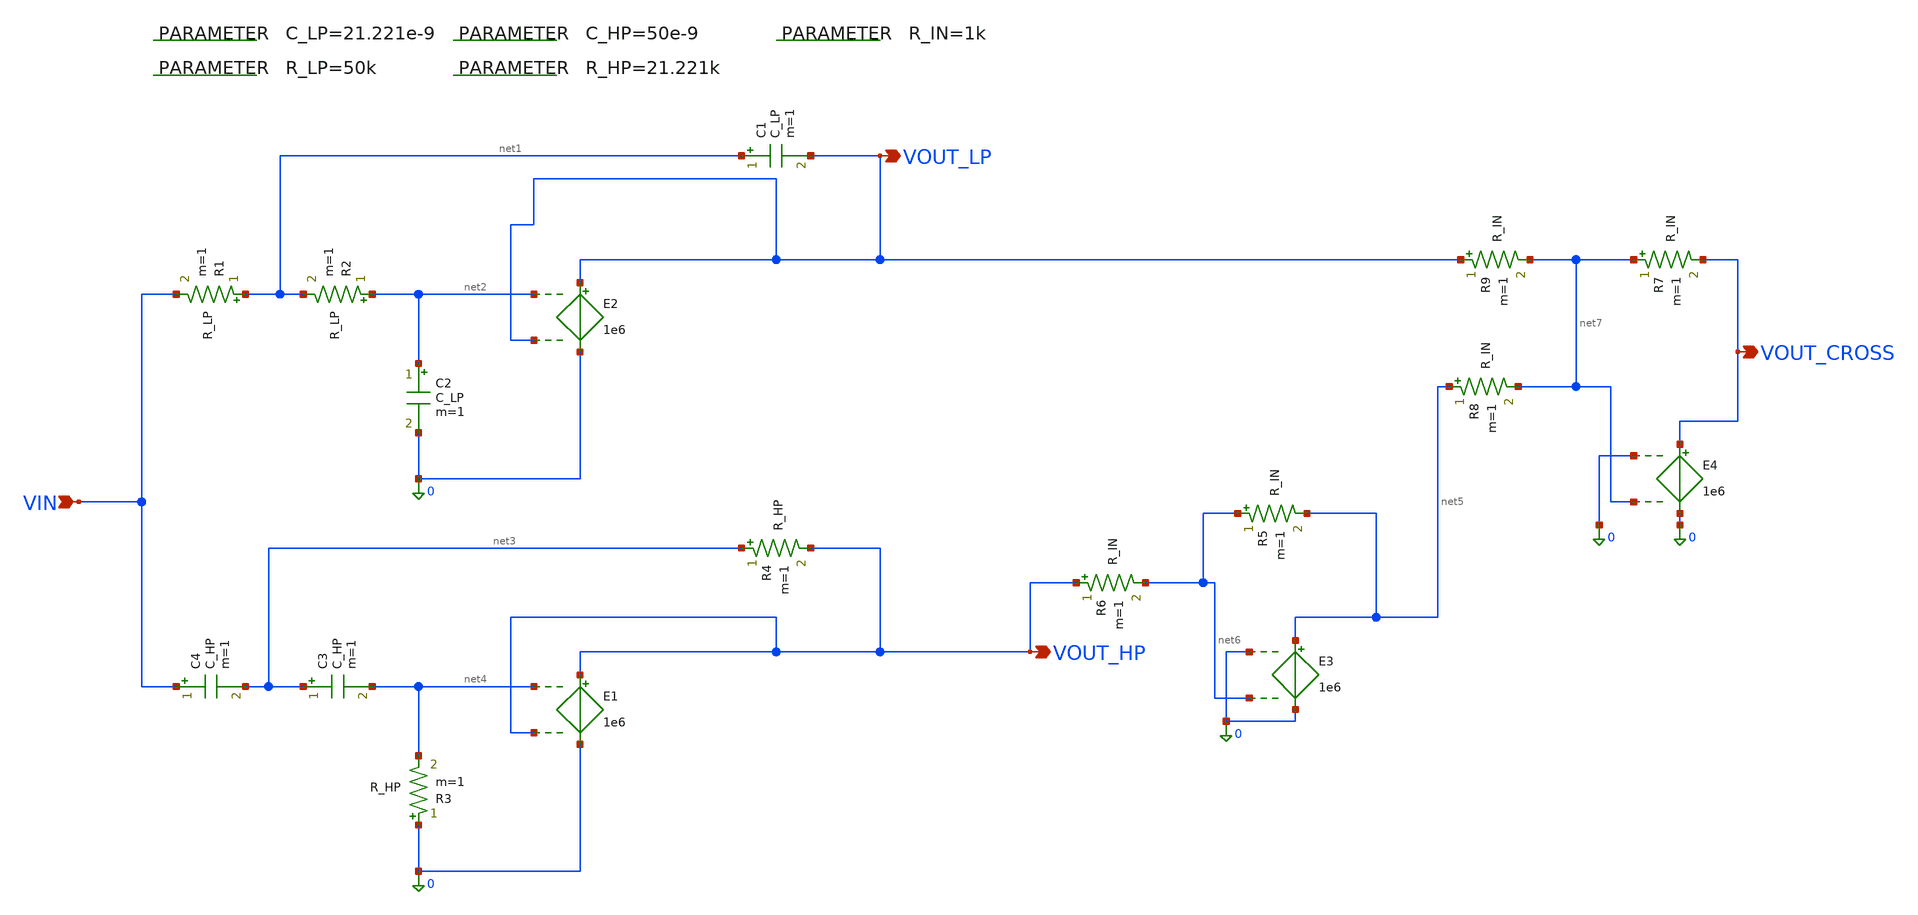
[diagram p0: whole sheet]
** sch_path: 003_Ideal_Circuits/linkwitz_riley_cross_vsvc_150hz.sch
**.subckt linkwitz_riley_cross_vsvc_150hz VIN VOUT_LP VOUT_HP VOUT_CROSS
*.ipin VIN
*.opin VOUT_LP
*.opin VOUT_HP
*.opin VOUT_CROSS
R1 net1 VIN R_LP m=1
R2 net2 net1 R_LP m=1
C1 net1 VOUT_LP C_LP m=1
C2 net2 0 C_LP m=1
.param C_LP=21.221e-9
.param R_LP=50k
R3 0 net4 R_HP m=1
R4 net3 VOUT_HP R_HP m=1
C3 net3 net4 C_HP m=1
C4 VIN net3 C_HP m=1
.param C_HP=50e-9
.param R_HP=21.221k
R5 net6 net5 R_IN m=1
R6 VOUT_HP net6 R_IN m=1
.param R_IN=1k
R7 net7 VOUT_CROSS R_IN m=1
R8 net5 net7 R_IN m=1
R9 VOUT_LP net7 R_IN m=1
E2 VOUT_LP 0 net2 VOUT_LP 1e6
E1 VOUT_HP 0 net4 VOUT_HP 1e6
E3 net5 0 0 net6 1e6
E4 VOUT_CROSS 0 0 net7 1e6
**.ends
.end
